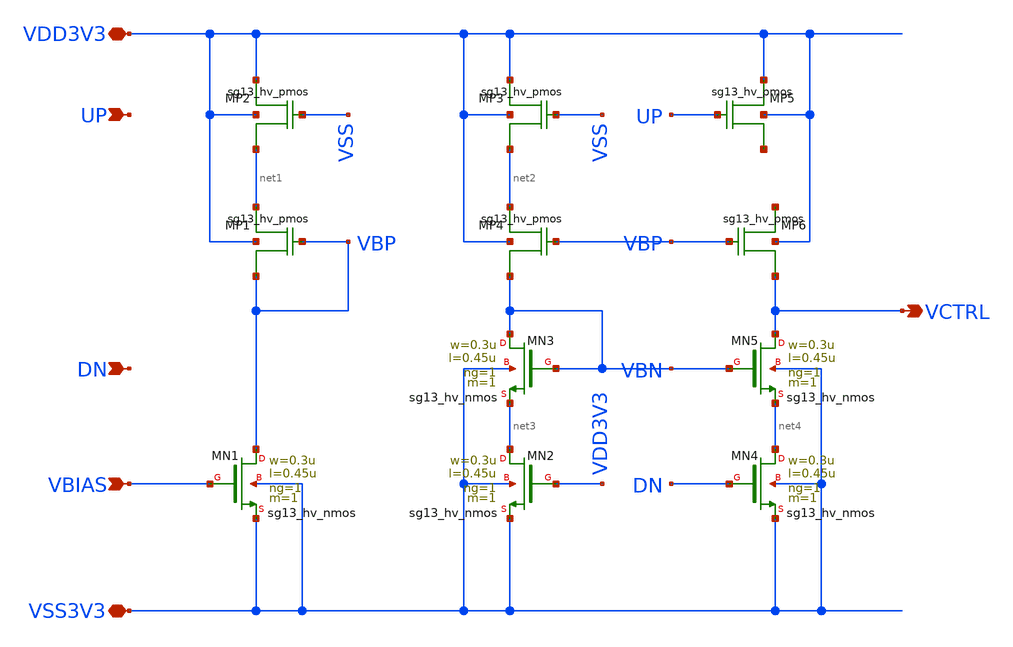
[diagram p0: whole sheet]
** sch_path: macros/pll_top/schematic/xschem/cp_top.sch
* Copyright (C) 1998-2024 Stefan Frederik Schippers
* This program is free software; you can redistribute it and/or modify
* it under the terms of the GNU General Public License as published by
* the Free Software Foundation; either version 2 of the License, or
* (at your option) any later version.
* This program is distributed in the hope that it will be useful,
* but WITHOUT ANY WARRANTY; without even the implied warranty of
* MERCHANTABILITY or FITNESS FOR A PARTICULAR PURPOSE.  See the
* GNU General Public License for more details.
* You should have received a copy of the GNU General Public License
* along with this program; if not, write to the Free Software
**.subckt cp_top VSS3V3 VDD3V3 UP DN VCTRL VBIAS
*.iopin VSS3V3
*.iopin VDD3V3
*.ipin UP
*.ipin DN
*.opin VCTRL
*.ipin VBIAS
XMN4 net4 DN VSS3V3 VSS3V3 sg13_hv_nmos w=0.3u l=0.45u ng=1 m=1 mm_ok=1
XMN5 VCTRL VBN net4 VSS3V3 sg13_hv_nmos w=0.3u l=0.45u ng=1 m=1 mm_ok=1
XMN1 VBP VBIAS VSS3V3 VSS3V3 sg13_hv_nmos w=0.3u l=0.45u ng=1 m=1 mm_ok=1
XMP1 net1 VBP VBP VDD3V3 sg13_hv_pmos w=0.3u l=0.4u ng=1 m=1
XMP2 VDD3V3 VSS net1 VDD3V3 sg13_hv_pmos w=0.3u l=0.4u ng=1 m=1
XMP3 VDD3V3 VSS net2 VDD3V3 sg13_hv_pmos w=0.3u l=0.4u ng=1 m=1
XMP4 net2 VBP VBN VDD3V3 sg13_hv_pmos w=0.3u l=0.4u ng=1 m=1
XMP6 net5 VBP VCTRL VDD3V3 sg13_hv_pmos w=0.3u l=0.4u ng=1 m=1
XMP5 VDD3V3 UP net6 VDD3V3 sg13_hv_pmos w=0.3u l=0.4u ng=1 m=1
XMN3 VBN VBN net3 VSS3V3 sg13_hv_nmos w=0.3u l=0.45u ng=1 m=1 mm_ok=1
XMN2 net3 VDD3V3 VSS3V3 VSS3V3 sg13_hv_nmos w=0.3u l=0.45u ng=1 m=1 mm_ok=1
**.ends
.end
